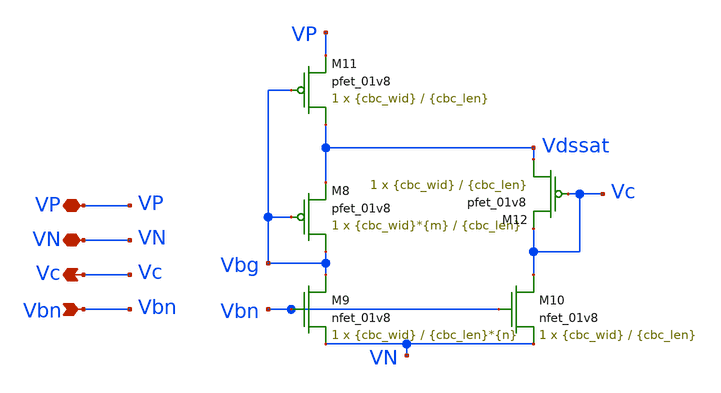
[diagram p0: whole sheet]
** sch_path: cbc.sch
**.subckt cbc VP VN Vc Vbn
*.iopin VP
*.iopin VN
*.opin Vc
*.ipin Vbn
XM8 Vbg Vbg Vdssat VP sky130_fd_pr__pfet_01v8 L={cbc_len} W={cbc_wid}*{m} nf=1 ad='int((nf+1)/2) * W/nf * 0.29'
+ as='int((nf+2)/2) * W/nf * 0.29' pd='2*int((nf+1)/2) * (W/nf + 0.29)' ps='2*int((nf+2)/2) * (W/nf + 0.29)'
+ nrd='0.29 / W' nrs='0.29 / W' sa=0 sb=0 sd=0 mult=1 m=1
XM9 Vbg Vbn VN VN sky130_fd_pr__nfet_01v8 L={cbc_len}*{n} W={cbc_wid} nf=1 ad='int((nf+1)/2) * W/nf * 0.29'
+ as='int((nf+2)/2) * W/nf * 0.29' pd='2*int((nf+1)/2) * (W/nf + 0.29)' ps='2*int((nf+2)/2) * (W/nf + 0.29)'
+ nrd='0.29 / W' nrs='0.29 / W' sa=0 sb=0 sd=0 mult=1 m=1
XM10 Vc Vbn VN VN sky130_fd_pr__nfet_01v8 L={cbc_len} W={cbc_wid} nf=1 ad='int((nf+1)/2) * W/nf * 0.29'
+ as='int((nf+2)/2) * W/nf * 0.29' pd='2*int((nf+1)/2) * (W/nf + 0.29)' ps='2*int((nf+2)/2) * (W/nf + 0.29)'
+ nrd='0.29 / W' nrs='0.29 / W' sa=0 sb=0 sd=0 mult=1 m=1
XM11 Vdssat Vbg VP VP sky130_fd_pr__pfet_01v8 L={cbc_len} W={cbc_wid} nf=1 ad='int((nf+1)/2) * W/nf * 0.29'
+ as='int((nf+2)/2) * W/nf * 0.29' pd='2*int((nf+1)/2) * (W/nf + 0.29)' ps='2*int((nf+2)/2) * (W/nf + 0.29)'
+ nrd='0.29 / W' nrs='0.29 / W' sa=0 sb=0 sd=0 mult=1 m=1
XM12 Vdssat Vc Vc VP sky130_fd_pr__pfet_01v8 L={cbc_len} W={cbc_wid} nf=1 ad='int((nf+1)/2) * W/nf * 0.29'
+ as='int((nf+2)/2) * W/nf * 0.29' pd='2*int((nf+1)/2) * (W/nf + 0.29)' ps='2*int((nf+2)/2) * (W/nf + 0.29)'
+ nrd='0.29 / W' nrs='0.29 / W' sa=0 sb=0 sd=0 mult=1 m=1
**.ends
.end
